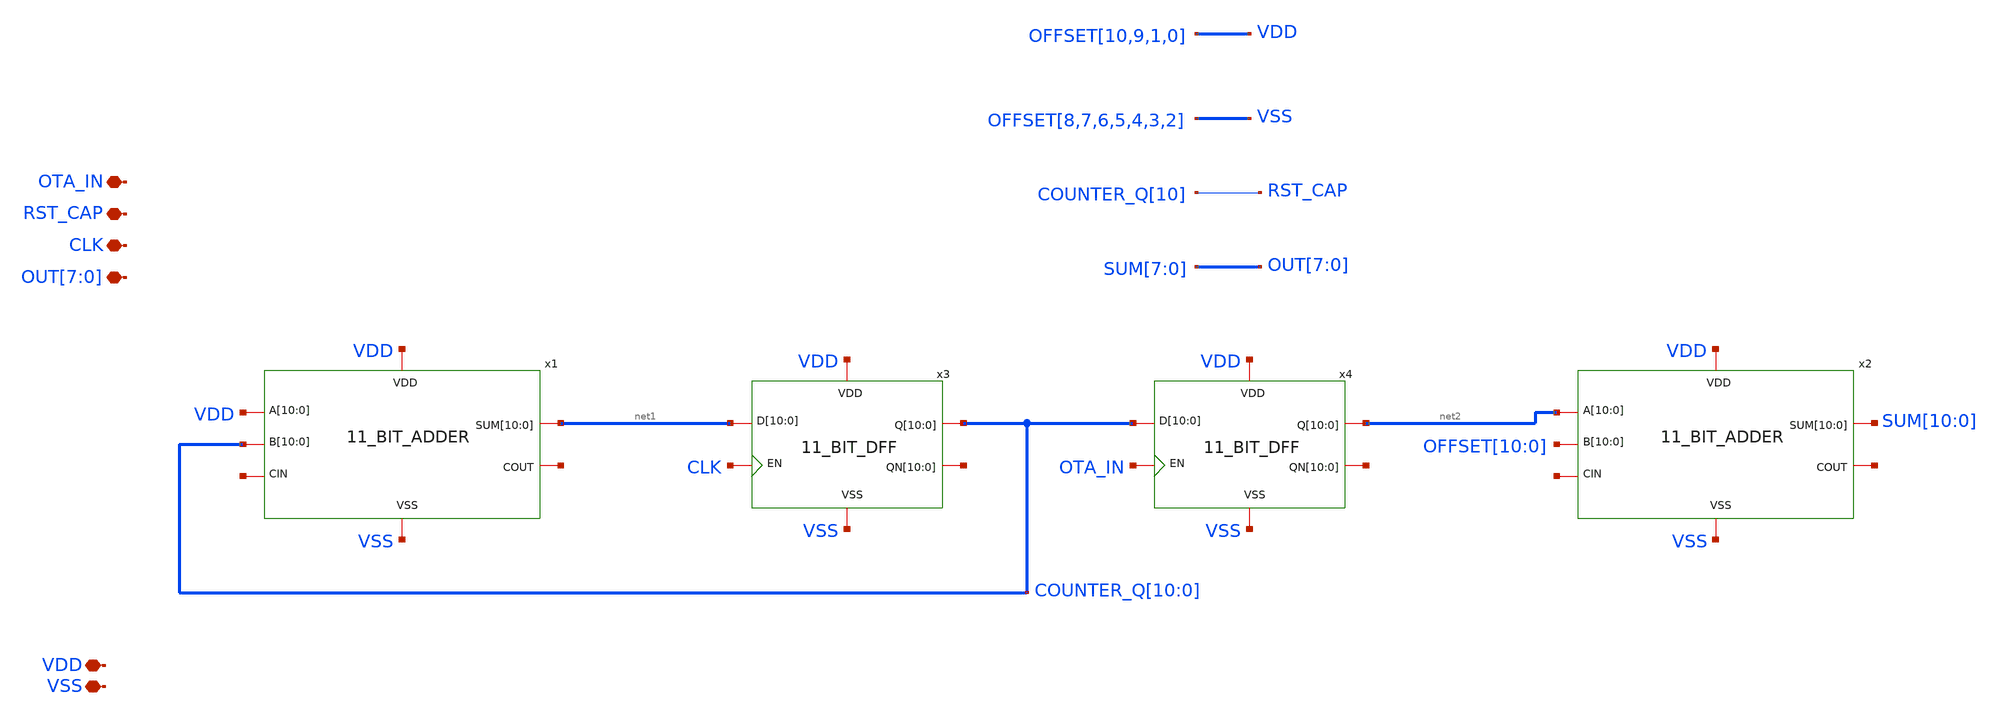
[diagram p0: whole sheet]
** sch_path: design/CNR_GR03_SKY130NM/MILESTONE3.sch
**.subckt MILESTONE3 VDD VSS OTA_IN RST_CAP CLK
*+ OUT[7],OUT[6],OUT[5],OUT[4],OUT[3],OUT[2],OUT[1],OUT[0]
*.iopin VDD
*.iopin VSS
*.iopin OTA_IN
*.iopin RST_CAP
*.iopin CLK
*.iopin OUT[7],OUT[6],OUT[5],OUT[4],OUT[3],OUT[2],OUT[1],OUT[0]
x1 net1[10] net1[9] net1[8] net1[7] net1[6] net1[5] net1[4] net1[3] net1[2] net1[1] net1[0] VDD VDD
+ VDD VDD VDD VDD VDD VDD VDD VDD VDD COUNTER_Q[10] COUNTER_Q[9] COUNTER_Q[8] COUNTER_Q[7] COUNTER_Q[6]
+ COUNTER_Q[5] COUNTER_Q[4] COUNTER_Q[3] COUNTER_Q[2] COUNTER_Q[1] COUNTER_Q[0] net3 net4 VDD VSS 11_BIT_ADDER
x2 SUM[10] SUM[9] SUM[8] SUM[7] SUM[6] SUM[5] SUM[4] SUM[3] SUM[2] SUM[1] SUM[0] net2[10] net2[9]
+ net2[8] net2[7] net2[6] net2[5] net2[4] net2[3] net2[2] net2[1] net2[0] OFFSET[10] OFFSET[9] OFFSET[8]
+ OFFSET[7] OFFSET[6] OFFSET[5] OFFSET[4] OFFSET[3] OFFSET[2] OFFSET[1] OFFSET[0] net5 net6 VDD VSS
+ 11_BIT_ADDER
x3 VDD VSS net1[10] net1[9] net1[8] net1[7] net1[6] net1[5] net1[4] net1[3] net1[2] net1[1] net1[0]
+ COUNTER_Q[10] COUNTER_Q[9] COUNTER_Q[8] COUNTER_Q[7] COUNTER_Q[6] COUNTER_Q[5] COUNTER_Q[4] COUNTER_Q[3]
+ COUNTER_Q[2] COUNTER_Q[1] COUNTER_Q[0] net7[10] net7[9] net7[8] net7[7] net7[6] net7[5] net7[4] net7[3] net7[2]
+ net7[1] net7[0] CLK 11_BIT_DFF
x4 VDD VSS COUNTER_Q[10] COUNTER_Q[9] COUNTER_Q[8] COUNTER_Q[7] COUNTER_Q[6] COUNTER_Q[5]
+ COUNTER_Q[4] COUNTER_Q[3] COUNTER_Q[2] COUNTER_Q[1] COUNTER_Q[0] net2[10] net2[9] net2[8] net2[7] net2[6]
+ net2[5] net2[4] net2[3] net2[2] net2[1] net2[0] net8[10] net8[9] net8[8] net8[7] net8[6] net8[5] net8[4]
+ net8[3] net8[2] net8[1] net8[0] OTA_IN 11_BIT_DFF
**.ends
.end
